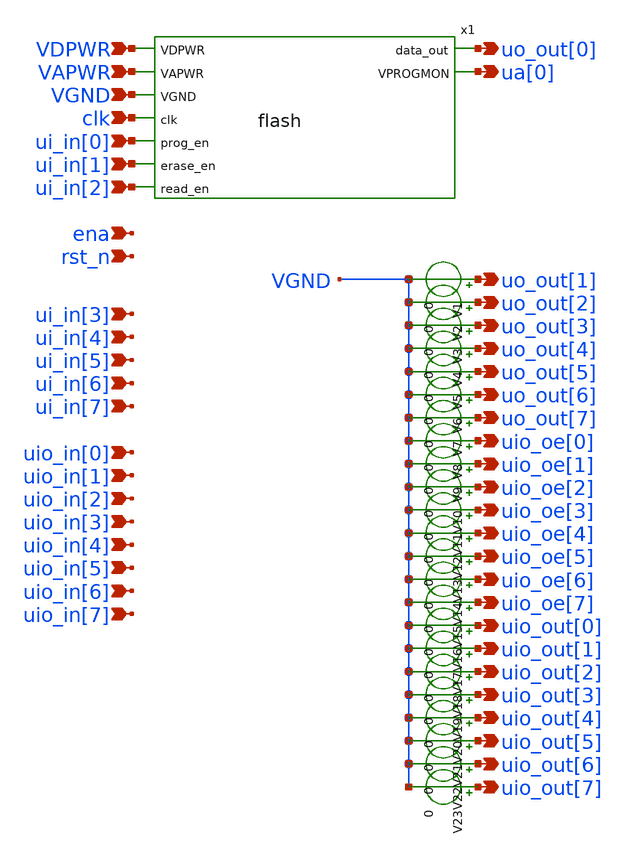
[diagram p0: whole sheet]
** sch_path: xschem/tt_um_sonos_flash_party.sch
**.subckt tt_um_sonos_flash_party VDPWR VAPWR VGND clk ui_in[0] ui_in[1] ui_in[2] uo_out[0] ua[0]
*+ uo_out[1] uo_out[2] uo_out[3] uo_out[4] uo_out[5] uo_out[6] uo_out[7] uio_oe[0] uio_oe[1] uio_oe[2] uio_oe[3]
*+ uio_oe[4] uio_oe[5] uio_oe[6] uio_oe[7] uio_out[0] uio_out[1] uio_out[2] uio_out[3] uio_out[4] uio_out[5]
*+ uio_out[6] uio_out[7] ui_in[3] ui_in[4] ui_in[5] ui_in[6] ui_in[7] uio_in[3] uio_in[4] uio_in[5] uio_in[6]
*+ uio_in[7] uio_in[0] uio_in[1] uio_in[2] rst_n ena
*.ipin VDPWR
*.ipin VAPWR
*.ipin VGND
*.ipin clk
*.ipin ui_in[0]
*.ipin ui_in[1]
*.ipin ui_in[2]
*.opin uo_out[0]
*.opin ua[0]
*.opin uo_out[1]
*.opin uo_out[2]
*.opin uo_out[3]
*.opin uo_out[4]
*.opin uo_out[5]
*.opin uo_out[6]
*.opin uo_out[7]
*.opin uio_oe[0]
*.opin uio_oe[1]
*.opin uio_oe[2]
*.opin uio_oe[3]
*.opin uio_oe[4]
*.opin uio_oe[5]
*.opin uio_oe[6]
*.opin uio_oe[7]
*.opin uio_out[0]
*.opin uio_out[1]
*.opin uio_out[2]
*.opin uio_out[3]
*.opin uio_out[4]
*.opin uio_out[5]
*.opin uio_out[6]
*.opin uio_out[7]
*.ipin ui_in[3]
*.ipin ui_in[4]
*.ipin ui_in[5]
*.ipin ui_in[6]
*.ipin ui_in[7]
*.ipin uio_in[3]
*.ipin uio_in[4]
*.ipin uio_in[5]
*.ipin uio_in[6]
*.ipin uio_in[7]
*.ipin uio_in[0]
*.ipin uio_in[1]
*.ipin uio_in[2]
*.ipin rst_n
*.ipin ena
x1 uo_out[0] VDPWR VAPWR VGND clk ua[0] ui_in[0] ui_in[1] ui_in[2] flash
V1 uo_out[1] VGND 0
V2 uo_out[2] VGND 0
V3 uo_out[3] VGND 0
V4 uo_out[4] VGND 0
V5 uo_out[5] VGND 0
V6 uo_out[6] VGND 0
V7 uo_out[7] VGND 0
V8 uio_oe[0] VGND 0
V9 uio_oe[1] VGND 0
V10 uio_oe[2] VGND 0
V11 uio_oe[3] VGND 0
V12 uio_oe[4] VGND 0
V13 uio_oe[5] VGND 0
V14 uio_oe[6] VGND 0
V15 uio_oe[7] VGND 0
V16 uio_out[0] VGND 0
V17 uio_out[1] VGND 0
V18 uio_out[2] VGND 0
V19 uio_out[3] VGND 0
V20 uio_out[4] VGND 0
V21 uio_out[5] VGND 0
V22 uio_out[6] VGND 0
V23 uio_out[7] VGND 0
**.ends
.end
